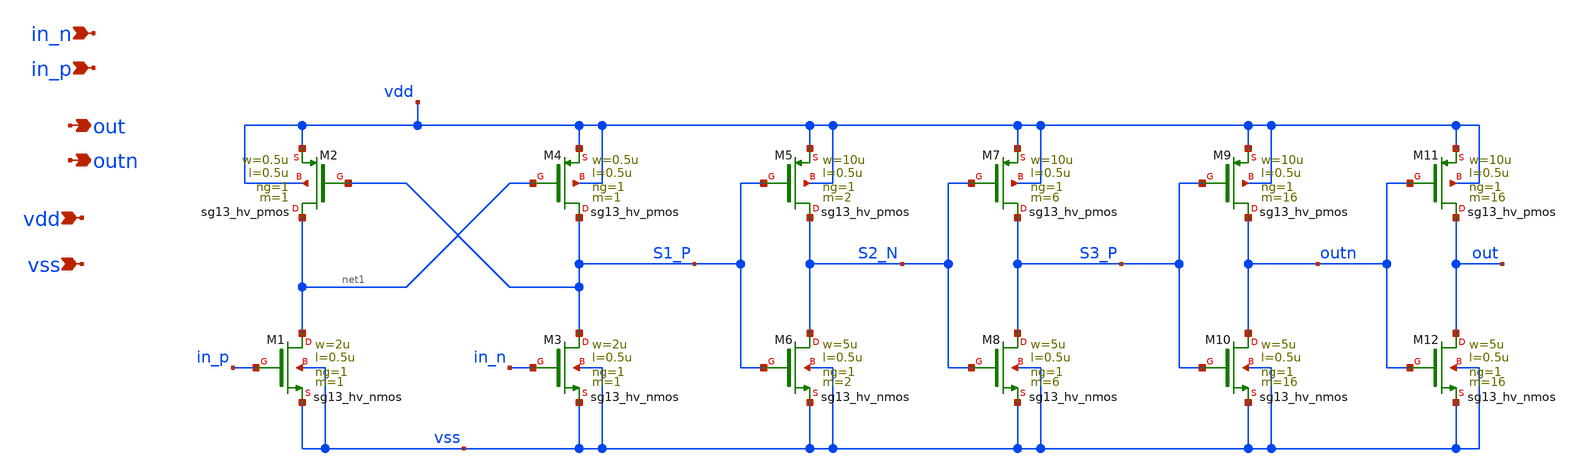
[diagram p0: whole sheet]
** sch_path: macros/ocd_analog_switches/schematic/xschem/gate_drive_med.sch
**.subckt gate_drive_med in_n in_p vdd vss out outn
*.ipin in_n
*.ipin in_p
*.ipin vdd
*.ipin vss
*.opin out
*.opin outn
XM1 net1 in_p vss vss sg13_hv_nmos w=2u l=0.5u ng=1 m=1 mm_ok=1
XM2 net1 S1_P vdd vdd sg13_hv_pmos w=0.5u l=0.5u ng=1 m=1 mm_ok=1
XM3 S1_P in_n vss vss sg13_hv_nmos w=2u l=0.5u ng=1 m=1 mm_ok=1
XM4 S1_P net1 vdd vdd sg13_hv_pmos w=0.5u l=0.5u ng=1 m=1 mm_ok=1
XM5 S2_N S1_P vdd vdd sg13_hv_pmos w=10u l=0.5u ng=1 m=2 mm_ok=1
XM6 S2_N S1_P vss vss sg13_hv_nmos w=5u l=0.5u ng=1 m=2 mm_ok=1
XM7 S3_P S2_N vdd vdd sg13_hv_pmos w=10u l=0.5u ng=1 m=6 mm_ok=1
XM8 S3_P S2_N vss vss sg13_hv_nmos w=5u l=0.5u ng=1 m=6 mm_ok=1
XM9 outn S3_P vdd vdd sg13_hv_pmos w=10u l=0.5u ng=1 m=16 mm_ok=1
XM10 outn S3_P vss vss sg13_hv_nmos w=5u l=0.5u ng=1 m=16 mm_ok=1
XM11 out outn vdd vdd sg13_hv_pmos w=10u l=0.5u ng=1 m=16 mm_ok=1
XM12 out outn vss vss sg13_hv_nmos w=5u l=0.5u ng=1 m=16 mm_ok=1
**.ends
.end
